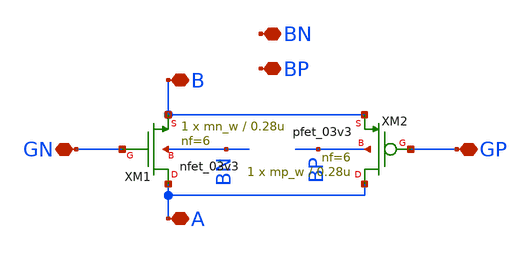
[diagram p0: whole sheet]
** sch_path: designs/switch_matrix_gf180mcu_9t5v0-main/tgate_PK/transmission_gate.sch
**.subckt transmission_gate B GN A GP BN BP
*.iopin B
*.iopin GN
*.iopin A
*.iopin GP
*.iopin BN
*.iopin BP
XM1 A GN B BN nfet_03v3 L=0.28u W=mn_w nf=6 ad='int((nf+1)/2) * W/nf * 0.18u' as='int((nf+2)/2) * W/nf * 0.18u'
+ pd='2*int((nf+1)/2) * (W/nf + 0.18u)' ps='2*int((nf+2)/2) * (W/nf + 0.18u)' nrd='0.18u / W' nrs='0.18u / W'
+ sa=0 sb=0 sd=0 m=1
XM2 A GP B BP pfet_03v3 L=0.28u W=mp_w nf=6 ad='int((nf+1)/2) * W/nf * 0.18u' as='int((nf+2)/2) * W/nf * 0.18u'
+ pd='2*int((nf+1)/2) * (W/nf + 0.18u)' ps='2*int((nf+2)/2) * (W/nf + 0.18u)' nrd='0.18u / W' nrs='0.18u / W'
+ sa=0 sb=0 sd=0 m=1
**.ends
.end
